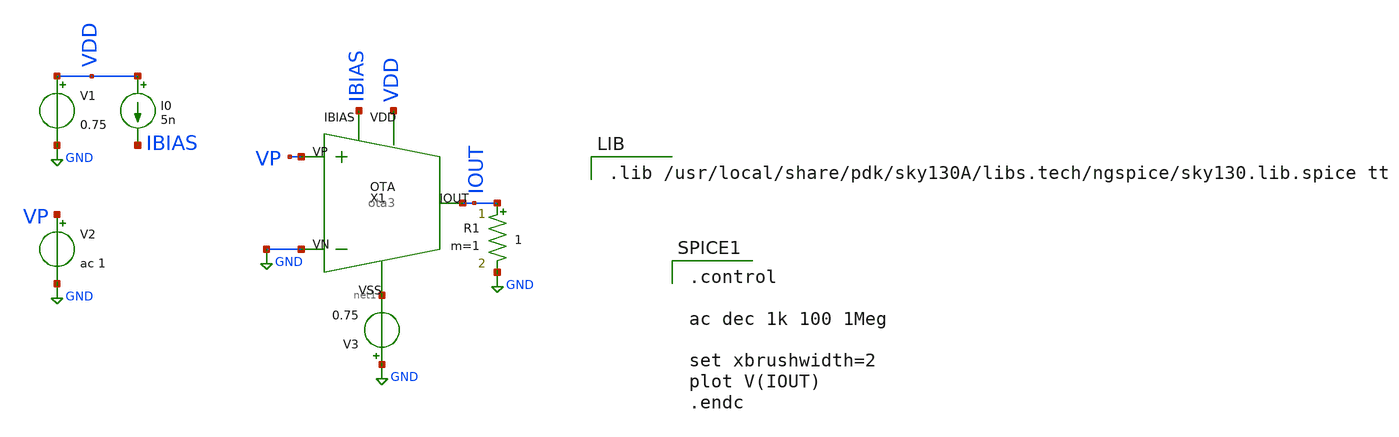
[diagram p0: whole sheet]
** sch_path: Fractional Order PID/OTA/ota3_tb.sch
**.subckt ota3_tb
V1 VDD GND 0.75
V2 VP GND ac 1
I0 VDD IBIAS 5n
V3 GND net1 0.75
R1 IOUT GND 1 m=1
X1 IBIAS VDD IOUT net1 GND VP ota3
**** begin user architecture code

.lib /usr/local/share/pdk/sky130A/libs.tech/ngspice/sky130.lib.spice tt


.control

ac dec 1k 100 1Meg

set xbrushwidth=2
plot V(IOUT)
.endc


**** end user architecture code
**.ends

* expanding   symbol:  /home/parallels/OTA/ota3.sym # of pins=6
** sym_path: Fractional Order PID/OTA/ota3.sym
** sch_path: Fractional Order PID/OTA/ota3.sch
.subckt ota3 IBIAS VDD IOUT VSS VN VP
*.iopin VP
*.iopin IBIAS
*.iopin IOUT
*.iopin VDD
*.iopin VSS
*.iopin VN
XMp1 net1 net1 VDD VDD sky130_fd_pr__pfet_01v8 L=2 W=10 nf=2 ad='int((nf+1)/2) * W/nf * 0.29' as='int((nf+2)/2) * W/nf * 0.29'
+ pd='2*int((nf+1)/2) * (W/nf + 0.29)' ps='2*int((nf+2)/2) * (W/nf + 0.29)' nrd='0.29 / W' nrs='0.29 / W'
+ sa=0 sb=0 sd=0 mult=1 m=1
XMp2 IOUT net1 VDD VDD sky130_fd_pr__pfet_01v8 L=2 W=10 nf=2 ad='int((nf+1)/2) * W/nf * 0.29' as='int((nf+2)/2) * W/nf * 0.29'
+ pd='2*int((nf+1)/2) * (W/nf + 0.29)' ps='2*int((nf+2)/2) * (W/nf + 0.29)' nrd='0.29 / W' nrs='0.29 / W'
+ sa=0 sb=0 sd=0 mult=1 m=1
XMn1 net1 VP net2 net2 sky130_fd_pr__nfet_01v8 L=5 W=25 nf=5 ad='int((nf+1)/2) * W/nf * 0.29' as='int((nf+2)/2) * W/nf * 0.29'
+ pd='2*int((nf+1)/2) * (W/nf + 0.29)' ps='2*int((nf+2)/2) * (W/nf + 0.29)' nrd='0.29 / W' nrs='0.29 / W'
+ sa=0 sb=0 sd=0 mult=1 m=1
XMn2 IOUT VN net2 net2 sky130_fd_pr__nfet_01v8 L=5 W=5 nf=1 ad='int((nf+1)/2) * W/nf * 0.29' as='int((nf+2)/2) * W/nf * 0.29'
+ pd='2*int((nf+1)/2) * (W/nf + 0.29)' ps='2*int((nf+2)/2) * (W/nf + 0.29)' nrd='0.29 / W' nrs='0.29 / W'
+ sa=0 sb=0 sd=0 mult=1 m=1
XMn3 net1 VP net3 net3 sky130_fd_pr__nfet_01v8 L=5 W=5 nf=1 ad='int((nf+1)/2) * W/nf * 0.29' as='int((nf+2)/2) * W/nf * 0.29'
+ pd='2*int((nf+1)/2) * (W/nf + 0.29)' ps='2*int((nf+2)/2) * (W/nf + 0.29)' nrd='0.29 / W' nrs='0.29 / W'
+ sa=0 sb=0 sd=0 mult=1 m=1
XMn4 IOUT VN net3 net3 sky130_fd_pr__nfet_01v8 L=5 W=25 nf=5 ad='int((nf+1)/2) * W/nf * 0.29' as='int((nf+2)/2) * W/nf * 0.29'
+ pd='2*int((nf+1)/2) * (W/nf + 0.29)' ps='2*int((nf+2)/2) * (W/nf + 0.29)' nrd='0.29 / W' nrs='0.29 / W'
+ sa=0 sb=0 sd=0 mult=1 m=1
XMb2 net2 IBIAS VSS VSS sky130_fd_pr__nfet_01v8 L=1.5 W=60 nf=12 ad='int((nf+1)/2) * W/nf * 0.29' as='int((nf+2)/2) * W/nf * 0.29'
+ pd='2*int((nf+1)/2) * (W/nf + 0.29)' ps='2*int((nf+2)/2) * (W/nf + 0.29)' nrd='0.29 / W' nrs='0.29 / W'
+ sa=0 sb=0 sd=0 mult=1 m=1
XMb1 IBIAS IBIAS VSS VSS sky130_fd_pr__nfet_01v8 L=1.5 W=60 nf=12 ad='int((nf+1)/2) * W/nf * 0.29' as='int((nf+2)/2) * W/nf * 0.29'
+ pd='2*int((nf+1)/2) * (W/nf + 0.29)' ps='2*int((nf+2)/2) * (W/nf + 0.29)' nrd='0.29 / W' nrs='0.29 / W'
+ sa=0 sb=0 sd=0 mult=1 m=1
XMb3 net3 IBIAS VSS VSS sky130_fd_pr__nfet_01v8 L=1.5 W=60 nf=12 ad='int((nf+1)/2) * W/nf * 0.29' as='int((nf+2)/2) * W/nf * 0.29'
+ pd='2*int((nf+1)/2) * (W/nf + 0.29)' ps='2*int((nf+2)/2) * (W/nf + 0.29)' nrd='0.29 / W' nrs='0.29 / W'
+ sa=0 sb=0 sd=0 mult=1 m=1
.ends

.GLOBAL GND
.end
